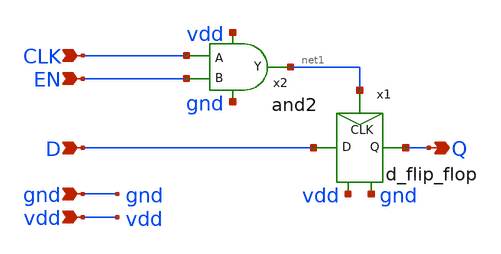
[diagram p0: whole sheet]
** sch_path: xschem/register.sch
**.subckt register CLK EN D Q vdd gnd
*.ipin CLK
*.ipin EN
*.ipin D
*.opin Q
*.ipin vdd
*.ipin gnd
x1 net1 Q D vdd gnd d_flip_flop
x2 CLK net1 EN vdd gnd vdd gnd and2
**.ends
.end
